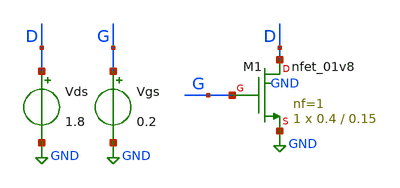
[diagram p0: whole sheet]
** sch_path: circuit_model/tb/dc_analysis.sch
**.subckt dc_analysis
Vds D GND 1.8
XM1 D G GND GND sky130_fd_pr__nfet_01v8 L=0.15 W=0.4 nf=1 ad='int((nf+1)/2) * W/nf * 0.29' as='int((nf+2)/2) * W/nf * 0.29'
+ pd='2*int((nf+1)/2) * (W/nf + 0.29)' ps='2*int((nf+2)/2) * (W/nf + 0.29)' nrd='0.29 / W' nrs='0.29 / W'
+ sa=0 sb=0 sd=0 mult=1 m=1
Vgs G GND 0.2
**** begin user architecture code


.lib /home/manhtd_61d/work/conda_eda/share/pdk/sky130A/libs.tech/ngspice/sky130.lib.spice tt

.control

* Measuring the threshold voltage of NMOS

let Id_ = vector(1810)
reshape Id_ [10][181]
compose Vg start = 0 stop = 2 step = 0.2
let j = 0
while Vg[j]<1.8
	echo "Vd sweeping"
	print j
	print Vgs[j]
	alter Vgs dc=Vg[j]
	dc Vds 0 1.8 0.01
	save i(Vds)
	let Id_[j]=-i(Vds)
	let j = j+1
end
let Id_0=Id_[0]
let Id_1=Id_[1]
let Id_2=Id_[2]
let Id_3=Id_[3]
let Id_4=Id_[4]
let Id_5=Id_[5]
let Id_6=Id_[6]
let Id_7=Id_[7]
let Id_8=Id_[8]
let Id_9=Id_[9]

write dc_analysis.raw
.endc


**** end user architecture code
**.ends
.GLOBAL GND
.end
